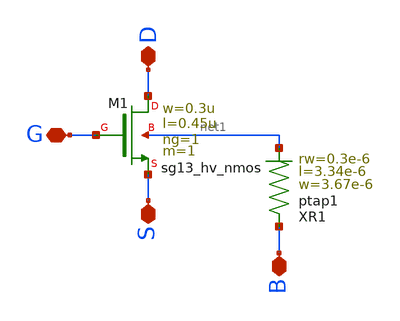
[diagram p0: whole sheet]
** sch_path: ihp-sg13cmos5l/schematic/xschem/sg13_hv_nmos_ring_pcell.sch
**.subckt sg13_hv_nmos_ring_pcell D S G B
*.iopin D
*.iopin S
*.iopin G
*.iopin B
XM1 D G S net1 sg13_hv_nmos w=0.3u l=0.45u ng=1 m=1 mm_ok=1
XR1 B net1 ptap1 R=17.78 w=3.67e-6 l=3.34e-6 rw=0.3e-6
**.ends
.end
